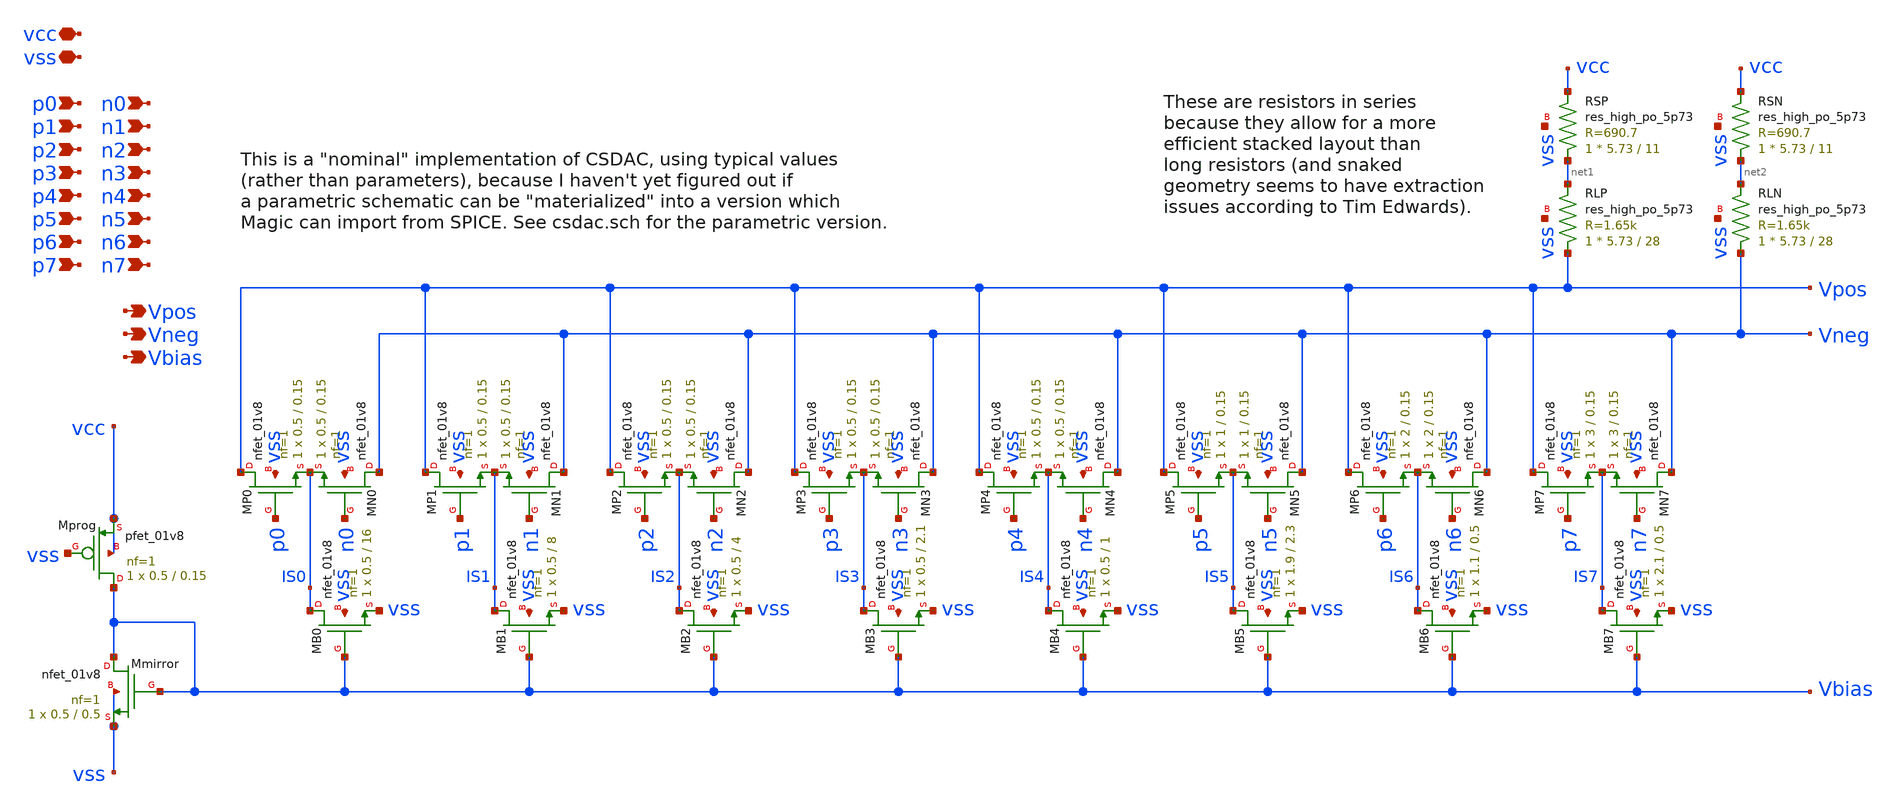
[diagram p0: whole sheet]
** sch_path: xschem/csdac_nom.sch
**.subckt csdac_nom vcc vss p0 n0 p1 n1 p2 n2 p3 n3 p4 n4 p5 n5 p6 n6 p7 n7 Vpos Vneg Vbias
*.iopin vcc
*.iopin vss
*.ipin p0
*.ipin n0
*.ipin p1
*.ipin n1
*.ipin p2
*.ipin n2
*.ipin p3
*.ipin n3
*.ipin p4
*.ipin n4
*.ipin p5
*.ipin n5
*.ipin p6
*.ipin n6
*.ipin p7
*.ipin n7
*.opin Vpos
*.opin Vneg
*.opin Vbias
XMprog Vbias vss vcc vcc sky130_fd_pr__pfet_01v8 L=0.15 W=0.5 nf=1 ad='int((nf+1)/2) * W/nf * 0.29' as='int((nf+2)/2) * W/nf * 0.29'
+ pd='2*int((nf+1)/2) * (W/nf + 0.29)' ps='2*int((nf+2)/2) * (W/nf + 0.29)' nrd='0.29 / W' nrs='0.29 / W'
+ sa=0 sb=0 sd=0 mult=1 m=1
XMmirror Vbias Vbias vss vss sky130_fd_pr__nfet_01v8 L=0.5 W=0.5 nf=1 ad='int((nf+1)/2) * W/nf * 0.29'
+ as='int((nf+2)/2) * W/nf * 0.29' pd='2*int((nf+1)/2) * (W/nf + 0.29)' ps='2*int((nf+2)/2) * (W/nf + 0.29)'
+ nrd='0.29 / W' nrs='0.29 / W' sa=0 sb=0 sd=0 mult=1 m=1
XMB0 IS0 Vbias vss vss sky130_fd_pr__nfet_01v8 L=16 W=0.5 nf=1 ad='int((nf+1)/2) * W/nf * 0.29' as='int((nf+2)/2) * W/nf * 0.29'
+ pd='2*int((nf+1)/2) * (W/nf + 0.29)' ps='2*int((nf+2)/2) * (W/nf + 0.29)' nrd='0.29 / W' nrs='0.29 / W'
+ sa=0 sb=0 sd=0 mult=1 m=1
XMP0 Vpos p0 IS0 vss sky130_fd_pr__nfet_01v8 L=0.15 W=0.5 nf=1 ad='int((nf+1)/2) * W/nf * 0.29' as='int((nf+2)/2) * W/nf * 0.29'
+ pd='2*int((nf+1)/2) * (W/nf + 0.29)' ps='2*int((nf+2)/2) * (W/nf + 0.29)' nrd='0.29 / W' nrs='0.29 / W'
+ sa=0 sb=0 sd=0 mult=1 m=1
XMN0 Vneg n0 IS0 vss sky130_fd_pr__nfet_01v8 L=0.15 W=0.5 nf=1 ad='int((nf+1)/2) * W/nf * 0.29' as='int((nf+2)/2) * W/nf * 0.29'
+ pd='2*int((nf+1)/2) * (W/nf + 0.29)' ps='2*int((nf+2)/2) * (W/nf + 0.29)' nrd='0.29 / W' nrs='0.29 / W'
+ sa=0 sb=0 sd=0 mult=1 m=1
XMB1 IS1 Vbias vss vss sky130_fd_pr__nfet_01v8 L=8 W=0.5 nf=1 ad='int((nf+1)/2) * W/nf * 0.29' as='int((nf+2)/2) * W/nf * 0.29'
+ pd='2*int((nf+1)/2) * (W/nf + 0.29)' ps='2*int((nf+2)/2) * (W/nf + 0.29)' nrd='0.29 / W' nrs='0.29 / W'
+ sa=0 sb=0 sd=0 mult=1 m=1
XMP1 Vpos p1 IS1 vss sky130_fd_pr__nfet_01v8 L=0.15 W=0.5 nf=1 ad='int((nf+1)/2) * W/nf * 0.29' as='int((nf+2)/2) * W/nf * 0.29'
+ pd='2*int((nf+1)/2) * (W/nf + 0.29)' ps='2*int((nf+2)/2) * (W/nf + 0.29)' nrd='0.29 / W' nrs='0.29 / W'
+ sa=0 sb=0 sd=0 mult=1 m=1
XMN1 Vneg n1 IS1 vss sky130_fd_pr__nfet_01v8 L=0.15 W=0.5 nf=1 ad='int((nf+1)/2) * W/nf * 0.29' as='int((nf+2)/2) * W/nf * 0.29'
+ pd='2*int((nf+1)/2) * (W/nf + 0.29)' ps='2*int((nf+2)/2) * (W/nf + 0.29)' nrd='0.29 / W' nrs='0.29 / W'
+ sa=0 sb=0 sd=0 mult=1 m=1
XMB2 IS2 Vbias vss vss sky130_fd_pr__nfet_01v8 L=4 W=0.5 nf=1 ad='int((nf+1)/2) * W/nf * 0.29' as='int((nf+2)/2) * W/nf * 0.29'
+ pd='2*int((nf+1)/2) * (W/nf + 0.29)' ps='2*int((nf+2)/2) * (W/nf + 0.29)' nrd='0.29 / W' nrs='0.29 / W'
+ sa=0 sb=0 sd=0 mult=1 m=1
XMP2 Vpos p2 IS2 vss sky130_fd_pr__nfet_01v8 L=0.15 W=0.5 nf=1 ad='int((nf+1)/2) * W/nf * 0.29' as='int((nf+2)/2) * W/nf * 0.29'
+ pd='2*int((nf+1)/2) * (W/nf + 0.29)' ps='2*int((nf+2)/2) * (W/nf + 0.29)' nrd='0.29 / W' nrs='0.29 / W'
+ sa=0 sb=0 sd=0 mult=1 m=1
XMN2 Vneg n2 IS2 vss sky130_fd_pr__nfet_01v8 L=0.15 W=0.5 nf=1 ad='int((nf+1)/2) * W/nf * 0.29' as='int((nf+2)/2) * W/nf * 0.29'
+ pd='2*int((nf+1)/2) * (W/nf + 0.29)' ps='2*int((nf+2)/2) * (W/nf + 0.29)' nrd='0.29 / W' nrs='0.29 / W'
+ sa=0 sb=0 sd=0 mult=1 m=1
XMB3 IS3 Vbias vss vss sky130_fd_pr__nfet_01v8 L=2.1 W=0.5 nf=1 ad='int((nf+1)/2) * W/nf * 0.29' as='int((nf+2)/2) * W/nf * 0.29'
+ pd='2*int((nf+1)/2) * (W/nf + 0.29)' ps='2*int((nf+2)/2) * (W/nf + 0.29)' nrd='0.29 / W' nrs='0.29 / W'
+ sa=0 sb=0 sd=0 mult=1 m=1
XMP3 Vpos p3 IS3 vss sky130_fd_pr__nfet_01v8 L=0.15 W=0.5 nf=1 ad='int((nf+1)/2) * W/nf * 0.29' as='int((nf+2)/2) * W/nf * 0.29'
+ pd='2*int((nf+1)/2) * (W/nf + 0.29)' ps='2*int((nf+2)/2) * (W/nf + 0.29)' nrd='0.29 / W' nrs='0.29 / W'
+ sa=0 sb=0 sd=0 mult=1 m=1
XMN3 Vneg n3 IS3 vss sky130_fd_pr__nfet_01v8 L=0.15 W=0.5 nf=1 ad='int((nf+1)/2) * W/nf * 0.29' as='int((nf+2)/2) * W/nf * 0.29'
+ pd='2*int((nf+1)/2) * (W/nf + 0.29)' ps='2*int((nf+2)/2) * (W/nf + 0.29)' nrd='0.29 / W' nrs='0.29 / W'
+ sa=0 sb=0 sd=0 mult=1 m=1
XMB4 IS4 Vbias vss vss sky130_fd_pr__nfet_01v8 L=1 W=0.5 nf=1 ad='int((nf+1)/2) * W/nf * 0.29' as='int((nf+2)/2) * W/nf * 0.29'
+ pd='2*int((nf+1)/2) * (W/nf + 0.29)' ps='2*int((nf+2)/2) * (W/nf + 0.29)' nrd='0.29 / W' nrs='0.29 / W'
+ sa=0 sb=0 sd=0 mult=1 m=1
XMP4 Vpos p4 IS4 vss sky130_fd_pr__nfet_01v8 L=0.15 W=0.5 nf=1 ad='int((nf+1)/2) * W/nf * 0.29' as='int((nf+2)/2) * W/nf * 0.29'
+ pd='2*int((nf+1)/2) * (W/nf + 0.29)' ps='2*int((nf+2)/2) * (W/nf + 0.29)' nrd='0.29 / W' nrs='0.29 / W'
+ sa=0 sb=0 sd=0 mult=1 m=1
XMN4 Vneg n4 IS4 vss sky130_fd_pr__nfet_01v8 L=0.15 W=0.5 nf=1 ad='int((nf+1)/2) * W/nf * 0.29' as='int((nf+2)/2) * W/nf * 0.29'
+ pd='2*int((nf+1)/2) * (W/nf + 0.29)' ps='2*int((nf+2)/2) * (W/nf + 0.29)' nrd='0.29 / W' nrs='0.29 / W'
+ sa=0 sb=0 sd=0 mult=1 m=1
XMB5 IS5 Vbias vss vss sky130_fd_pr__nfet_01v8 L=2.3 W=1.9 nf=1 ad='int((nf+1)/2) * W/nf * 0.29' as='int((nf+2)/2) * W/nf * 0.29'
+ pd='2*int((nf+1)/2) * (W/nf + 0.29)' ps='2*int((nf+2)/2) * (W/nf + 0.29)' nrd='0.29 / W' nrs='0.29 / W'
+ sa=0 sb=0 sd=0 mult=1 m=1
XMP5 Vpos p5 IS5 vss sky130_fd_pr__nfet_01v8 L=0.15 W=1 nf=1 ad='int((nf+1)/2) * W/nf * 0.29' as='int((nf+2)/2) * W/nf * 0.29'
+ pd='2*int((nf+1)/2) * (W/nf + 0.29)' ps='2*int((nf+2)/2) * (W/nf + 0.29)' nrd='0.29 / W' nrs='0.29 / W'
+ sa=0 sb=0 sd=0 mult=1 m=1
XMN5 Vneg n5 IS5 vss sky130_fd_pr__nfet_01v8 L=0.15 W=1 nf=1 ad='int((nf+1)/2) * W/nf * 0.29' as='int((nf+2)/2) * W/nf * 0.29'
+ pd='2*int((nf+1)/2) * (W/nf + 0.29)' ps='2*int((nf+2)/2) * (W/nf + 0.29)' nrd='0.29 / W' nrs='0.29 / W'
+ sa=0 sb=0 sd=0 mult=1 m=1
XMB6 IS6 Vbias vss vss sky130_fd_pr__nfet_01v8 L=0.5 W=1.1 nf=1 ad='int((nf+1)/2) * W/nf * 0.29' as='int((nf+2)/2) * W/nf * 0.29'
+ pd='2*int((nf+1)/2) * (W/nf + 0.29)' ps='2*int((nf+2)/2) * (W/nf + 0.29)' nrd='0.29 / W' nrs='0.29 / W'
+ sa=0 sb=0 sd=0 mult=1 m=1
XMP6 Vpos p6 IS6 vss sky130_fd_pr__nfet_01v8 L=0.15 W=2 nf=1 ad='int((nf+1)/2) * W/nf * 0.29' as='int((nf+2)/2) * W/nf * 0.29'
+ pd='2*int((nf+1)/2) * (W/nf + 0.29)' ps='2*int((nf+2)/2) * (W/nf + 0.29)' nrd='0.29 / W' nrs='0.29 / W'
+ sa=0 sb=0 sd=0 mult=1 m=1
XMN6 Vneg n6 IS6 vss sky130_fd_pr__nfet_01v8 L=0.15 W=2 nf=1 ad='int((nf+1)/2) * W/nf * 0.29' as='int((nf+2)/2) * W/nf * 0.29'
+ pd='2*int((nf+1)/2) * (W/nf + 0.29)' ps='2*int((nf+2)/2) * (W/nf + 0.29)' nrd='0.29 / W' nrs='0.29 / W'
+ sa=0 sb=0 sd=0 mult=1 m=1
XMB7 IS7 Vbias vss vss sky130_fd_pr__nfet_01v8 L=0.5 W=2.1 nf=1 ad='int((nf+1)/2) * W/nf * 0.29' as='int((nf+2)/2) * W/nf * 0.29'
+ pd='2*int((nf+1)/2) * (W/nf + 0.29)' ps='2*int((nf+2)/2) * (W/nf + 0.29)' nrd='0.29 / W' nrs='0.29 / W'
+ sa=0 sb=0 sd=0 mult=1 m=1
XMP7 Vpos p7 IS7 vss sky130_fd_pr__nfet_01v8 L=0.15 W=3 nf=1 ad='int((nf+1)/2) * W/nf * 0.29' as='int((nf+2)/2) * W/nf * 0.29'
+ pd='2*int((nf+1)/2) * (W/nf + 0.29)' ps='2*int((nf+2)/2) * (W/nf + 0.29)' nrd='0.29 / W' nrs='0.29 / W'
+ sa=0 sb=0 sd=0 mult=1 m=1
XMN7 Vneg n7 IS7 vss sky130_fd_pr__nfet_01v8 L=0.15 W=3 nf=1 ad='int((nf+1)/2) * W/nf * 0.29' as='int((nf+2)/2) * W/nf * 0.29'
+ pd='2*int((nf+1)/2) * (W/nf + 0.29)' ps='2*int((nf+2)/2) * (W/nf + 0.29)' nrd='0.29 / W' nrs='0.29 / W'
+ sa=0 sb=0 sd=0 mult=1 m=1
XRLP Vpos net1 vss sky130_fd_pr__res_high_po_5p73 L=28 mult=1 m=1
XRLN Vneg net2 vss sky130_fd_pr__res_high_po_5p73 L=28 mult=1 m=1
XRSP net1 vcc vss sky130_fd_pr__res_high_po_5p73 L=11 mult=1 m=1
XRSN net2 vcc vss sky130_fd_pr__res_high_po_5p73 L=11 mult=1 m=1
**.ends
.end
